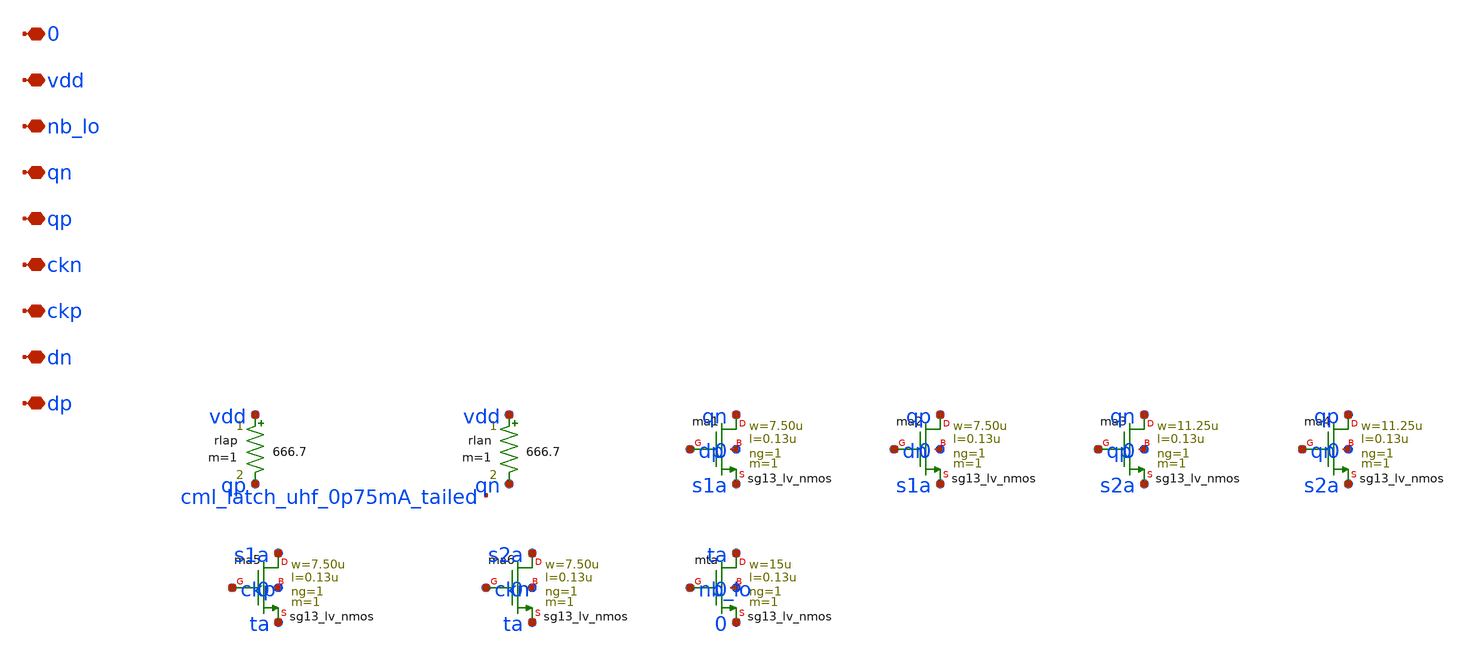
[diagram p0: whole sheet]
** sch_path: analog/lo/sch/cml_latch_uhf.sch
**.subckt cml_latch_uhf dp dn ckp ckn qp qn nb_lo vdd 0
*.iopin dp
*.iopin dn
*.iopin ckp
*.iopin ckn
*.iopin qp
*.iopin qn
*.iopin nb_lo
*.iopin vdd
*.iopin 0
rlap vdd qp 666.7 m=1
rlan vdd qn 666.7 m=1
Xma1 qn dp s1a 0 sg13_lv_nmos w=7.50u l=0.13u ng=1 m=1 mm_ok=1
Xma2 qp dn s1a 0 sg13_lv_nmos w=7.50u l=0.13u ng=1 m=1 mm_ok=1
Xma3 qn qp s2a 0 sg13_lv_nmos w=11.25u l=0.13u ng=1 m=1 mm_ok=1
Xma4 qp qn s2a 0 sg13_lv_nmos w=11.25u l=0.13u ng=1 m=1 mm_ok=1
Xma5 s1a ckp ta 0 sg13_lv_nmos w=7.50u l=0.13u ng=1 m=1 mm_ok=1
Xma6 s2a ckn ta 0 sg13_lv_nmos w=7.50u l=0.13u ng=1 m=1 mm_ok=1
Xmta ta nb_lo 0 0 sg13_lv_nmos w=15u l=0.13u ng=1 m=1 mm_ok=1
**.ends
.end
